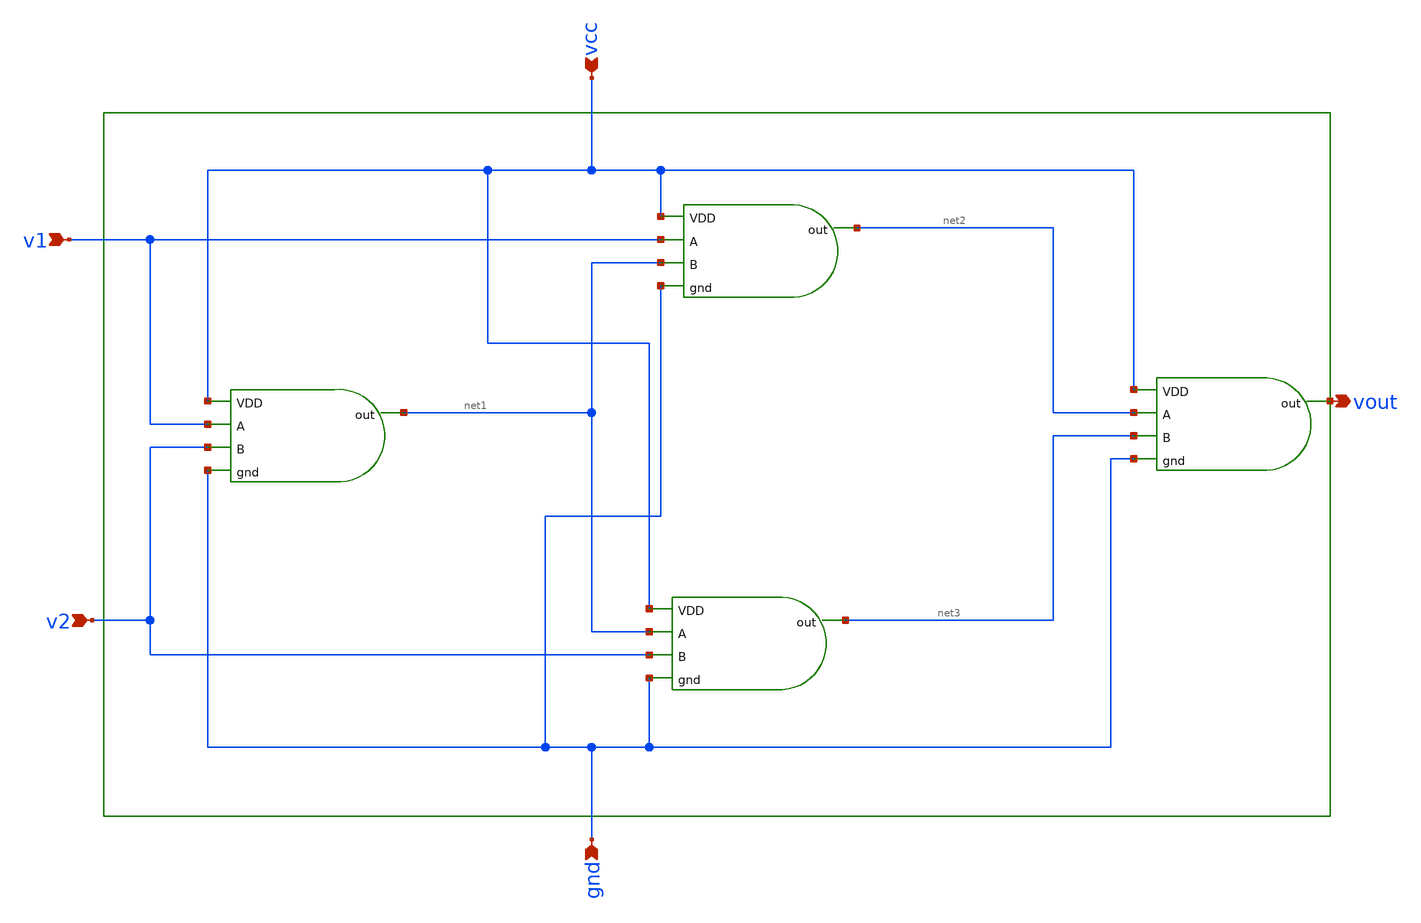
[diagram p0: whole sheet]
** sch_path: Logic_gates_using_cmos/xor_sg.sch
**.subckt xor_sg vcc vout v1 v2 gnd
*.ipin vcc
*.opin vout
*.ipin v1
*.ipin v2
*.ipin gnd
x2 vcc v1 net2 net1 gnd Nand_Cmos
x3 vcc net2 vout net3 gnd Nand_Cmos
x4 vcc net1 net3 v2 gnd Nand_Cmos
x1 vcc v1 net1 v2 gnd Nand_Cmos
**.ends

* expanding   symbol:  xschem_circuits/Nand_Cmos.sym # of pins=5
** sym_path: Logic_gates_using_cmos/Nand_Cmos.sym
** sch_path: Logic_gates_using_cmos/Nand_Cmos.sch
.subckt Nand_Cmos VDD A out B gnd
*.ipin B
*.ipin A
*.ipin VDD
*.ipin gnd
*.opin out
XM2 net2 A VDD VDD sky130_fd_pr__pfet_01v8 L=0.15 W=4 nf=1 ad='int((nf+1)/2) * W/nf * 0.29' as='int((nf+2)/2) * W/nf * 0.29'
+ pd='2*int((nf+1)/2) * (W/nf + 0.29)' ps='2*int((nf+2)/2) * (W/nf + 0.29)' nrd='0.29 / W' nrs='0.29 / W'
+ sa=0 sb=0 sd=0 mult=1 m=1
XM1 net2 A net1 gnd sky130_fd_pr__nfet_01v8 L=0.15 W=2 nf=1 ad='int((nf+1)/2) * W/nf * 0.29' as='int((nf+2)/2) * W/nf * 0.29'
+ pd='2*int((nf+1)/2) * (W/nf + 0.29)' ps='2*int((nf+2)/2) * (W/nf + 0.29)' nrd='0.29 / W' nrs='0.29 / W'
+ sa=0 sb=0 sd=0 mult=1 m=1
XM3 net1 B gnd gnd sky130_fd_pr__nfet_01v8 L=0.15 W=2 nf=1 ad='int((nf+1)/2) * W/nf * 0.29' as='int((nf+2)/2) * W/nf * 0.29'
+ pd='2*int((nf+1)/2) * (W/nf + 0.29)' ps='2*int((nf+2)/2) * (W/nf + 0.29)' nrd='0.29 / W' nrs='0.29 / W'
+ sa=0 sb=0 sd=0 mult=1 m=1
XM4 net2 B VDD VDD sky130_fd_pr__pfet_01v8 L=0.15 W=4 nf=1 ad='int((nf+1)/2) * W/nf * 0.29' as='int((nf+2)/2) * W/nf * 0.29'
+ pd='2*int((nf+1)/2) * (W/nf + 0.29)' ps='2*int((nf+2)/2) * (W/nf + 0.29)' nrd='0.29 / W' nrs='0.29 / W'
+ sa=0 sb=0 sd=0 mult=1 m=1
C1 out gnd 0.12p m=1
R1 out net2 40 m=1
.ends

.end
